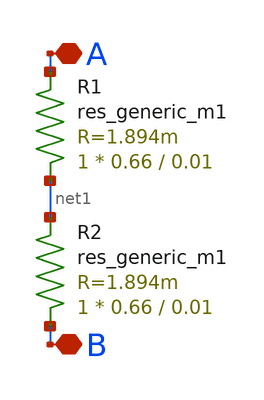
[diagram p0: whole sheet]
** sch_path: common/tk_em1s.sch
* Copyright 2023 David Mitchell Bailey
* Licensed under the Apache License, Version 2.0 (the "License");
* you may not use this file except in compliance with the License.
* You may obtain a copy of the License at
* https://www.apache.org/licenses/LICENSE-2.0
* Unless required by applicable law or agreed to in writing, software
* distributed under the License is distributed on an "AS IS" BASIS,
* WITHOUT WARRANTIES OR CONDITIONS OF ANY KIND, either express or implied.
* See the License for the specific language governing permissions and
* limitations under the License.
**.subckt tk_em1s A B
*.iopin A
*.iopin B
R1 net1 A sky130_fd_pr__res_generic_m1 W=0.66 L=0.01 m=1
R2 B net1 sky130_fd_pr__res_generic_m1 W=0.66 L=0.01 m=1
**.ends
.end
